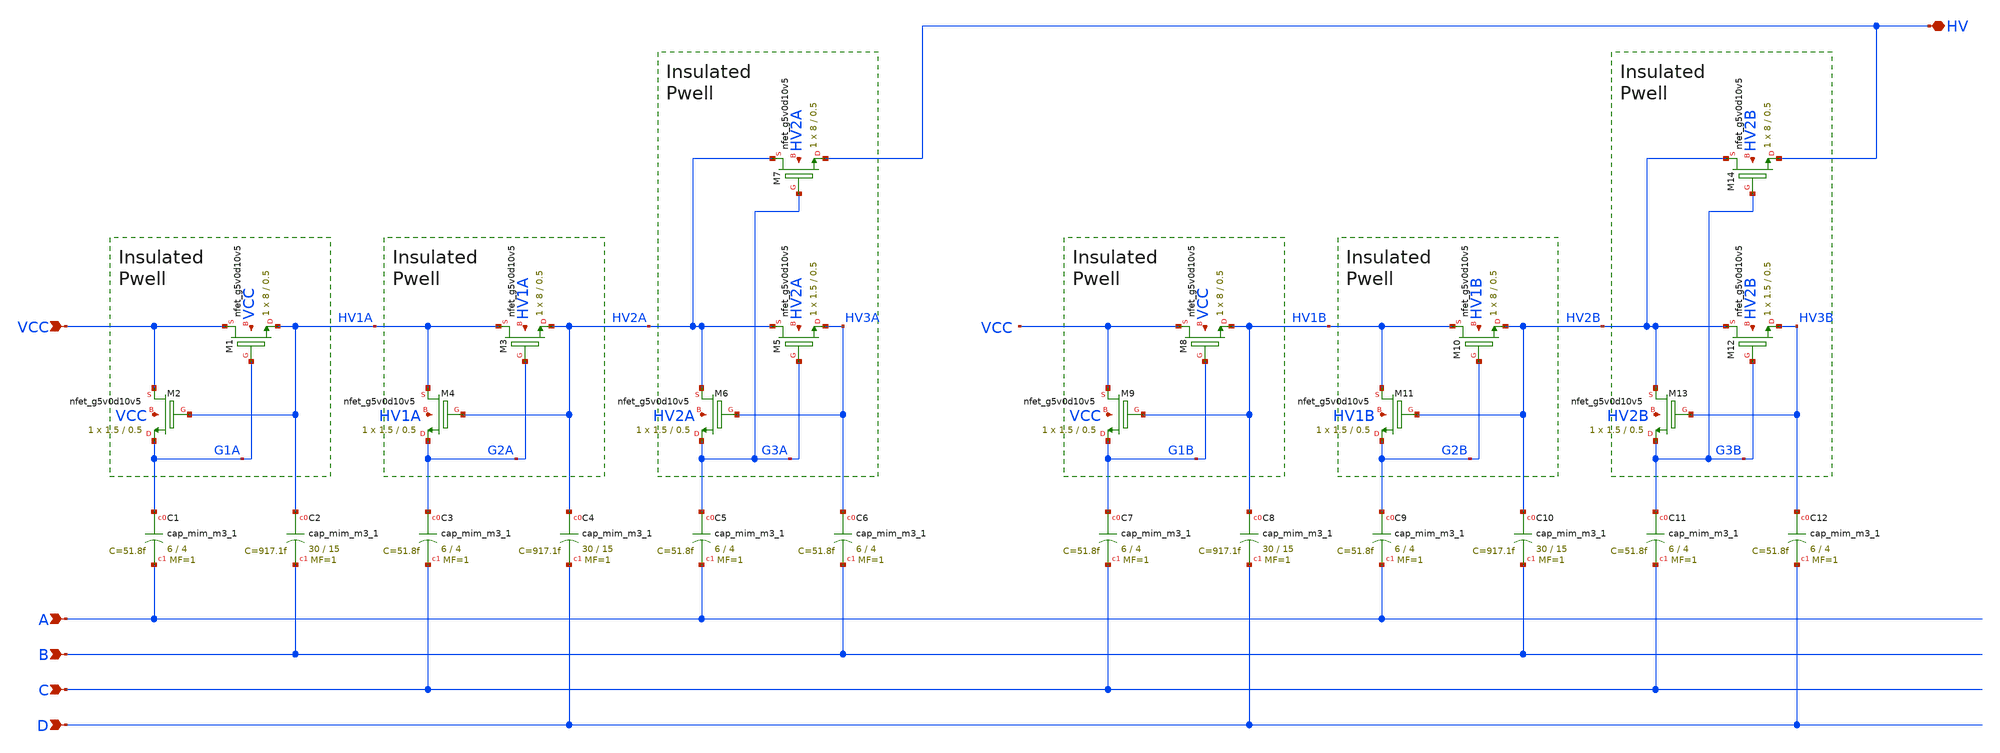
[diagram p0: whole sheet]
** sch_path: sky130_tests/charge_pump.sch
* Copyright 2021 Stefan Frederik Schippers
* Licensed under the Apache License, Version 2.0 (the "License");
* you may not use this file except in compliance with the License.
* You may obtain a copy of the License at
* https://www.apache.org/licenses/LICENSE-2.0
* Unless required by applicable law or agreed to in writing, software
* distributed under the License is distributed on an "AS IS" BASIS,
* WITHOUT WARRANTIES OR CONDITIONS OF ANY KIND, either express or implied.
* See the License for the specific language governing permissions and
* limitations under the License.
**.subckt charge_pump A B C D VCC HV
*.ipin A
*.ipin B
*.ipin C
*.ipin D
*.ipin VCC
*.iopin HV
XM1 VCC G1A HV1A VCC sky130_fd_pr__nfet_g5v0d10v5 W=8 L=0.5 ad='int((nf+1)/2) * W/nf * 0.29' pd='2*int((nf+1)/2) * (W/nf + 0.29)'
+ as='int((nf+2)/2) * W/nf * 0.29' ps='2*int((nf+2)/2) * (W/nf + 0.29)' nrd='0.29 / W' nrs='0.29 / W' sa=0
+ sb=0 sd=0 nf=1 mult=1
XM2 VCC HV1A G1A VCC sky130_fd_pr__nfet_g5v0d10v5 W=1.5 L=0.5 ad='int((nf+1)/2) * W/nf * 0.29' pd='2*int((nf+1)/2) * (W/nf + 0.29)'
+ as='int((nf+2)/2) * W/nf * 0.29' ps='2*int((nf+2)/2) * (W/nf + 0.29)' nrd='0.29 / W' nrs='0.29 / W' sa=0
+ sb=0 sd=0 nf=1 mult=1
XM3 HV1A G2A HV2A HV1A sky130_fd_pr__nfet_g5v0d10v5 W=8 L=0.5 ad='int((nf+1)/2) * W/nf * 0.29' pd='2*int((nf+1)/2) * (W/nf + 0.29)'
+ as='int((nf+2)/2) * W/nf * 0.29' ps='2*int((nf+2)/2) * (W/nf + 0.29)' nrd='0.29 / W' nrs='0.29 / W' sa=0
+ sb=0 sd=0 nf=1 mult=1
XM4 HV1A HV2A G2A HV1A sky130_fd_pr__nfet_g5v0d10v5 W=1.5 L=0.5 ad='int((nf+1)/2) * W/nf * 0.29' pd='2*int((nf+1)/2) * (W/nf + 0.29)'
+ as='int((nf+2)/2) * W/nf * 0.29' ps='2*int((nf+2)/2) * (W/nf + 0.29)' nrd='0.29 / W' nrs='0.29 / W' sa=0
+ sb=0 sd=0 nf=1 mult=1
XM5 HV2A G3A HV3A HV2A sky130_fd_pr__nfet_g5v0d10v5 W=1.5 L=0.5 ad='int((nf+1)/2) * W/nf * 0.29' pd='2*int((nf+1)/2) * (W/nf + 0.29)'
+ as='int((nf+2)/2) * W/nf * 0.29' ps='2*int((nf+2)/2) * (W/nf + 0.29)' nrd='0.29 / W' nrs='0.29 / W' sa=0
+ sb=0 sd=0 nf=1 mult=1
XM6 HV2A HV3A G3A HV2A sky130_fd_pr__nfet_g5v0d10v5 W=1.5 L=0.5 ad='int((nf+1)/2) * W/nf * 0.29' pd='2*int((nf+1)/2) * (W/nf + 0.29)'
+ as='int((nf+2)/2) * W/nf * 0.29' ps='2*int((nf+2)/2) * (W/nf + 0.29)' nrd='0.29 / W' nrs='0.29 / W' sa=0
+ sb=0 sd=0 nf=1 mult=1
XM7 HV2A G3A HV HV2A sky130_fd_pr__nfet_g5v0d10v5 W=8 L=0.5 ad='int((nf+1)/2) * W/nf * 0.29' pd='2*int((nf+1)/2) * (W/nf + 0.29)'
+ as='int((nf+2)/2) * W/nf * 0.29' ps='2*int((nf+2)/2) * (W/nf + 0.29)' nrd='0.29 / W' nrs='0.29 / W' sa=0
+ sb=0 sd=0 nf=1 mult=1
XC1 G1A A sky130_fd_pr__cap_mim_m3_1 W=6 L=4 MF=1 m=1
XC2 HV1A B sky130_fd_pr__cap_mim_m3_1 W=30 L=15 MF=1 m=1
XC3 G2A C sky130_fd_pr__cap_mim_m3_1 W=6 L=4 MF=1 m=1
XC4 HV2A D sky130_fd_pr__cap_mim_m3_1 W=30 L=15 MF=1 m=1
XC5 G3A A sky130_fd_pr__cap_mim_m3_1 W=6 L=4 MF=1 m=1
XC6 HV3A B sky130_fd_pr__cap_mim_m3_1 W=6 L=4 MF=1 m=1
XM8 VCC G1B HV1B VCC sky130_fd_pr__nfet_g5v0d10v5 W=8 L=0.5 ad='int((nf+1)/2) * W/nf * 0.29' pd='2*int((nf+1)/2) * (W/nf + 0.29)'
+ as='int((nf+2)/2) * W/nf * 0.29' ps='2*int((nf+2)/2) * (W/nf + 0.29)' nrd='0.29 / W' nrs='0.29 / W' sa=0
+ sb=0 sd=0 nf=1 mult=1
XM9 VCC HV1B G1B VCC sky130_fd_pr__nfet_g5v0d10v5 W=1.5 L=0.5 ad='int((nf+1)/2) * W/nf * 0.29' pd='2*int((nf+1)/2) * (W/nf + 0.29)'
+ as='int((nf+2)/2) * W/nf * 0.29' ps='2*int((nf+2)/2) * (W/nf + 0.29)' nrd='0.29 / W' nrs='0.29 / W' sa=0
+ sb=0 sd=0 nf=1 mult=1
XM10 HV1B G2B HV2B HV1B sky130_fd_pr__nfet_g5v0d10v5 W=8 L=0.5 ad='int((nf+1)/2) * W/nf * 0.29' pd='2*int((nf+1)/2) * (W/nf + 0.29)'
+ as='int((nf+2)/2) * W/nf * 0.29' ps='2*int((nf+2)/2) * (W/nf + 0.29)' nrd='0.29 / W' nrs='0.29 / W' sa=0
+ sb=0 sd=0 nf=1 mult=1
XM11 HV1B HV2B G2B HV1B sky130_fd_pr__nfet_g5v0d10v5 W=1.5 L=0.5 ad='int((nf+1)/2) * W/nf * 0.29' pd='2*int((nf+1)/2) * (W/nf + 0.29)'
+ as='int((nf+2)/2) * W/nf * 0.29' ps='2*int((nf+2)/2) * (W/nf + 0.29)' nrd='0.29 / W' nrs='0.29 / W' sa=0
+ sb=0 sd=0 nf=1 mult=1
XM12 HV2B G3B HV3B HV2B sky130_fd_pr__nfet_g5v0d10v5 W=1.5 L=0.5 ad='int((nf+1)/2) * W/nf * 0.29' pd='2*int((nf+1)/2) * (W/nf + 0.29)'
+ as='int((nf+2)/2) * W/nf * 0.29' ps='2*int((nf+2)/2) * (W/nf + 0.29)' nrd='0.29 / W' nrs='0.29 / W' sa=0
+ sb=0 sd=0 nf=1 mult=1
XM13 HV2B HV3B G3B HV2B sky130_fd_pr__nfet_g5v0d10v5 W=1.5 L=0.5 ad='int((nf+1)/2) * W/nf * 0.29' pd='2*int((nf+1)/2) * (W/nf + 0.29)'
+ as='int((nf+2)/2) * W/nf * 0.29' ps='2*int((nf+2)/2) * (W/nf + 0.29)' nrd='0.29 / W' nrs='0.29 / W' sa=0
+ sb=0 sd=0 nf=1 mult=1
XM14 HV2B G3B HV HV2B sky130_fd_pr__nfet_g5v0d10v5 W=8 L=0.5 ad='int((nf+1)/2) * W/nf * 0.29' pd='2*int((nf+1)/2) * (W/nf + 0.29)'
+ as='int((nf+2)/2) * W/nf * 0.29' ps='2*int((nf+2)/2) * (W/nf + 0.29)' nrd='0.29 / W' nrs='0.29 / W' sa=0
+ sb=0 sd=0 nf=1 mult=1
XC7 G1B C sky130_fd_pr__cap_mim_m3_1 W=6 L=4 MF=1 m=1
XC8 HV1B D sky130_fd_pr__cap_mim_m3_1 W=30 L=15 MF=1 m=1
XC9 G2B A sky130_fd_pr__cap_mim_m3_1 W=6 L=4 MF=1 m=1
XC10 HV2B B sky130_fd_pr__cap_mim_m3_1 W=30 L=15 MF=1 m=1
XC11 G3B C sky130_fd_pr__cap_mim_m3_1 W=6 L=4 MF=1 m=1
XC12 HV3B D sky130_fd_pr__cap_mim_m3_1 W=6 L=4 MF=1 m=1
**.ends
.end
